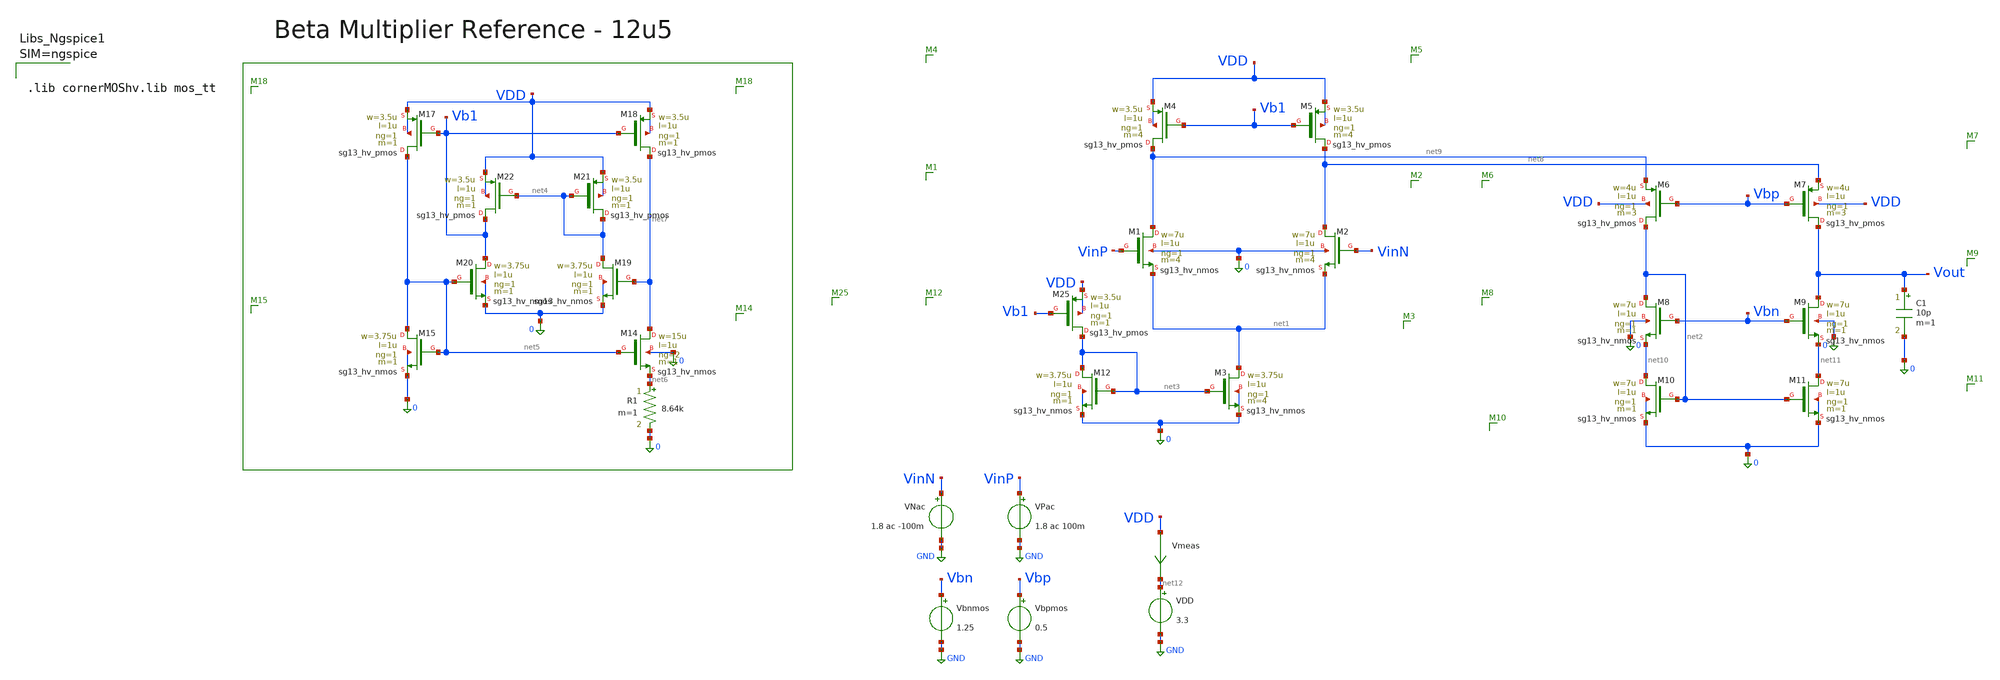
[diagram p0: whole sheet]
** sch_path: v2_bmr_bias/OP.sch
**.subckt OP
XM1 net9 VinP net1 0 sg13_hv_nmos w=7u l=1u ng=1 m=4 mm_ok=1
XM2 net8 VinN net1 0 sg13_hv_nmos w=7u l=1u ng=1 m=4 mm_ok=1
XM3 net1 net3 0 0 sg13_hv_nmos w=3.75u l=1u ng=1 m=4 mm_ok=1
XM4 net9 Vb1 VDD VDD sg13_hv_pmos w=3.5u l=1u ng=1 m=4 mm_ok=1
XM5 net8 Vb1 VDD VDD sg13_hv_pmos w=3.5u l=1u ng=1 m=4 mm_ok=1
XM6 net2 Vbp net9 VDD sg13_hv_pmos w=4u l=1u ng=1 m=3 mm_ok=1
XM7 Vout Vbp net8 VDD sg13_hv_pmos w=4u l=1u ng=1 m=3 mm_ok=1
XM8 net2 Vbn net10 0 sg13_hv_nmos w=7u l=1u ng=1 m=1 mm_ok=1
XM9 Vout Vbn net11 0 sg13_hv_nmos w=7u l=1u ng=1 m=1 mm_ok=1
XM10 net10 net2 0 0 sg13_hv_nmos w=7u l=1u ng=1 m=1 mm_ok=1
XM11 net11 net2 0 0 sg13_hv_nmos w=7u l=1u ng=1 m=1 mm_ok=1
VPac VinP GND 1.8 ac 100m
VNac VinN GND 1.8 ac -100m
Vbnmos Vbn GND 1.25
Vbpmos Vbp GND 0.5
C1 Vout 0 10p m=1
VDD net12 GND 3.3
XM25 net3 Vb1 VDD VDD sg13_hv_pmos w=3.5u l=1u ng=1 m=1 mm_ok=1
XM12 net3 net3 0 0 sg13_hv_nmos w=3.75u l=1u ng=1 m=1 mm_ok=1
R1 net6 0 8.64k m=1
XM14 net7 net5 net6 0 sg13_hv_nmos w=15u l=1u ng=2 m=1 mm_ok=1
XM15 net5 net5 0 0 sg13_hv_nmos w=3.75u l=1u ng=1 m=1 mm_ok=1
XM17 net5 Vb1 VDD VDD sg13_hv_pmos w=3.5u l=1u ng=1 m=1 mm_ok=1
XM18 net7 Vb1 VDD VDD sg13_hv_pmos w=3.5u l=1u ng=1 m=1 mm_ok=1
XM19 net4 net7 0 0 sg13_hv_nmos w=3.75u l=1u ng=1 m=1 mm_ok=1
XM20 Vb1 net5 0 0 sg13_hv_nmos w=3.75u l=1u ng=1 m=1 mm_ok=1
XM21 net4 net4 VDD VDD sg13_hv_pmos w=3.5u l=1u ng=1 m=1 mm_ok=1
XM22 Vb1 net4 VDD VDD sg13_hv_pmos w=3.5u l=1u ng=1 m=1 mm_ok=1
Vmeas VDD net12 0
.save i(vmeas)
**** begin user architecture code


.include OP.save
.control
op
write OP.raw
.endc





.lib cornerMOShv.lib mos_tt



**** end user architecture code
**.ends
.GLOBAL GND
.end
